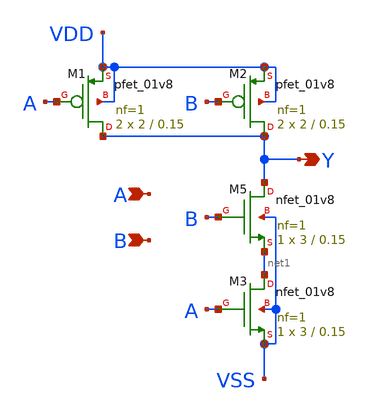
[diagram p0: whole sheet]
** sch_path: current/xschem/NAND2X1.sch
**.subckt NAND2X1 Y A B
*.opin Y
*.ipin A
*.ipin B
XM1 Y A VDD VDD sky130_fd_pr__pfet_01v8 L=0.15 W=2 nf=1 ad='int((nf+1)/2) * W/nf * 0.29' as='int((nf+2)/2) * W/nf * 0.29'
+ pd='2*int((nf+1)/2) * (W/nf + 0.29)' ps='2*int((nf+2)/2) * (W/nf + 0.29)' nrd='0.29 / W' nrs='0.29 / W'
+ sa=0 sb=0 sd=0 mult=2 m=2
XM5 Y B net1 VSS sky130_fd_pr__nfet_01v8 L=0.15 W=3 nf=1 ad='int((nf+1)/2) * W/nf * 0.29' as='int((nf+2)/2) * W/nf * 0.29'
+ pd='2*int((nf+1)/2) * (W/nf + 0.29)' ps='2*int((nf+2)/2) * (W/nf + 0.29)' nrd='0.29 / W' nrs='0.29 / W'
+ sa=0 sb=0 sd=0 mult=1 m=1
XM2 Y B VDD VDD sky130_fd_pr__pfet_01v8 L=0.15 W=2 nf=1 ad='int((nf+1)/2) * W/nf * 0.29' as='int((nf+2)/2) * W/nf * 0.29'
+ pd='2*int((nf+1)/2) * (W/nf + 0.29)' ps='2*int((nf+2)/2) * (W/nf + 0.29)' nrd='0.29 / W' nrs='0.29 / W'
+ sa=0 sb=0 sd=0 mult=2 m=2
XM3 net1 A VSS VSS sky130_fd_pr__nfet_01v8 L=0.15 W=3 nf=1 ad='int((nf+1)/2) * W/nf * 0.29' as='int((nf+2)/2) * W/nf * 0.29'
+ pd='2*int((nf+1)/2) * (W/nf + 0.29)' ps='2*int((nf+2)/2) * (W/nf + 0.29)' nrd='0.29 / W' nrs='0.29 / W'
+ sa=0 sb=0 sd=0 mult=1 m=1
**.ends
.end
